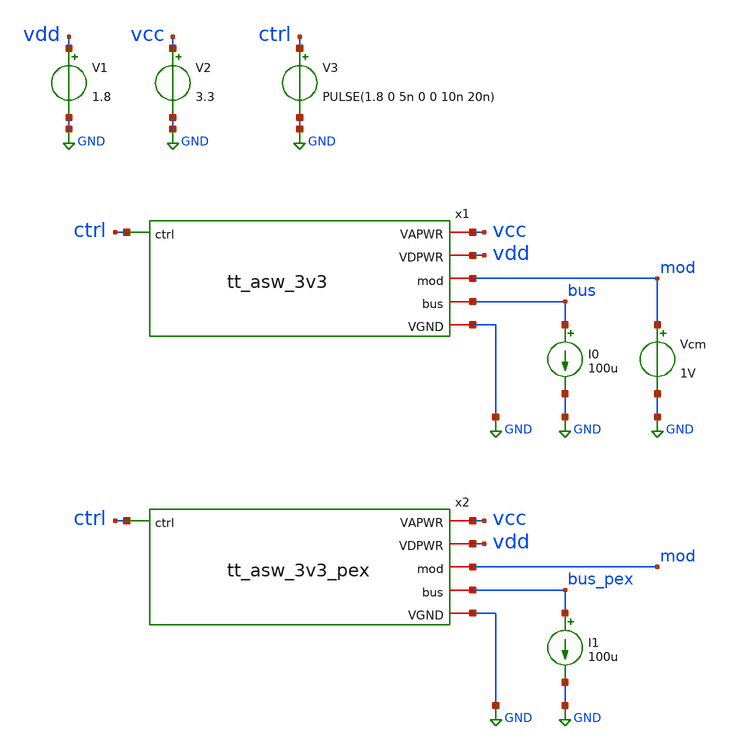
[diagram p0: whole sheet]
** sch_path: asw/tt_asw_3v3/xschem/tb_rdson.sch
**.subckt tb_rdson
x1 GND vdd vcc ctrl mod bus tt_asw_3v3
V2 vcc GND 3.3
Vcm mod GND 1V
I0 bus GND 100u
V3 ctrl GND PULSE(1.8 0 5n 0 0 10n 20n)
V1 vdd GND 1.8
x2 GND vdd vcc ctrl mod bus_pex tt_asw_3v3_pex
I1 bus_pex GND 100u
**** begin user architecture code

** opencircuitdesign pdks install
.lib $::SKYWATER_MODELS/sky130.lib.spice tt
.include $::SKYWATER_STDCELLS/sky130_fd_sc_hd.spice





.param mc_mm_switch=0
.control
tran 10p 100n
plot ctrl x1.tgon x1.tgon_n
dc Vcm 0 3.3 0.01
plot ((v(mod) - v(bus)) / 100u) ((v(mod) - v(bus_pex)) / 100u)
write tb_rdson.raw
*quit 0
.endc
.end


**** end user architecture code
**.ends

* expanding   symbol:  tt_asw_3v3.sym # of pins=6
** sym_path: asw/sky130/tt_asw_3v3/xschem/tt_asw_3v3.sym
** sch_path: asw/sky130/tt_asw_3v3/xschem/tt_asw_3v3.sch
.subckt tt_asw_3v3 VGND VDPWR VAPWR ctrl mod bus
*.iopin mod
*.iopin bus
*.ipin ctrl
*.iopin VGND
*.iopin VDPWR
*.iopin VAPWR
XM1 tgon_n net2 VAPWR VAPWR sky130_fd_pr__pfet_g5v0d10v5 L=0.5 W=0.84 nf=1 ad='int((nf+1)/2) * W/nf * 0.29'
+ as='int((nf+2)/2) * W/nf * 0.29' pd='2*int((nf+1)/2) * (W/nf + 0.29)' ps='2*int((nf+2)/2) * (W/nf + 0.29)'
+ nrd='0.29 / W' nrs='0.29 / W' sa=0 sb=0 sd=0 mult=1 m=1
XM2 tgon_n net2 VGND VGND sky130_fd_pr__nfet_g5v0d10v5 L=0.5 W=0.42 nf=1 ad='int((nf+1)/2) * W/nf * 0.29'
+ as='int((nf+2)/2) * W/nf * 0.29' pd='2*int((nf+1)/2) * (W/nf + 0.29)' ps='2*int((nf+2)/2) * (W/nf + 0.29)'
+ nrd='0.29 / W' nrs='0.29 / W' sa=0 sb=0 sd=0 mult=1 m=1
XM3 tgon net1 VAPWR VAPWR sky130_fd_pr__pfet_g5v0d10v5 L=0.5 W=0.84 nf=1 ad='int((nf+1)/2) * W/nf * 0.29'
+ as='int((nf+2)/2) * W/nf * 0.29' pd='2*int((nf+1)/2) * (W/nf + 0.29)' ps='2*int((nf+2)/2) * (W/nf + 0.29)'
+ nrd='0.29 / W' nrs='0.29 / W' sa=0 sb=0 sd=0 mult=1 m=1
XM4 tgon net1 VGND VGND sky130_fd_pr__nfet_g5v0d10v5 L=0.5 W=0.42 nf=1 ad='int((nf+1)/2) * W/nf * 0.29'
+ as='int((nf+2)/2) * W/nf * 0.29' pd='2*int((nf+1)/2) * (W/nf + 0.29)' ps='2*int((nf+2)/2) * (W/nf + 0.29)'
+ nrd='0.29 / W' nrs='0.29 / W' sa=0 sb=0 sd=0 mult=1 m=1
XM5 bus tgon_n mod VAPWR sky130_fd_pr__pfet_g5v0d10v5 L=0.5 W=180 nf=18 ad='int((nf+1)/2) * W/nf * 0.29'
+ as='int((nf+2)/2) * W/nf * 0.29' pd='2*int((nf+1)/2) * (W/nf + 0.29)' ps='2*int((nf+2)/2) * (W/nf + 0.29)'
+ nrd='0.29 / W' nrs='0.29 / W' sa=0 sb=0 sd=0 mult=1 m=1
XM6 bus tgon mod VGND sky130_fd_pr__nfet_g5v0d10v5 L=0.5 W=60 nf=12 ad='int((nf+1)/2) * W/nf * 0.29'
+ as='int((nf+2)/2) * W/nf * 0.29' pd='2*int((nf+1)/2) * (W/nf + 0.29)' ps='2*int((nf+2)/2) * (W/nf + 0.29)'
+ nrd='0.29 / W' nrs='0.29 / W' sa=0 sb=0 sd=0 mult=1 m=1
XM7 ctrl_n ctrl VGND VGND sky130_fd_pr__nfet_01v8 L=0.15 W=0.42 nf=1 ad='int((nf+1)/2) * W/nf * 0.29'
+ as='int((nf+2)/2) * W/nf * 0.29' pd='2*int((nf+1)/2) * (W/nf + 0.29)' ps='2*int((nf+2)/2) * (W/nf + 0.29)'
+ nrd='0.29 / W' nrs='0.29 / W' sa=0 sb=0 sd=0 mult=1 m=1
XM8 ctrl_n ctrl VDPWR VDPWR sky130_fd_pr__pfet_01v8_hvt L=0.15 W=1 nf=1 ad='int((nf+1)/2) * W/nf * 0.29'
+ as='int((nf+2)/2) * W/nf * 0.29' pd='2*int((nf+1)/2) * (W/nf + 0.29)' ps='2*int((nf+2)/2) * (W/nf + 0.29)'
+ nrd='0.29 / W' nrs='0.29 / W' sa=0 sb=0 sd=0 mult=1 m=1
XM9 net1 ctrl VGND VGND sky130_fd_pr__nfet_g5v0d10v5 L=0.5 W=0.42 nf=1 ad='int((nf+1)/2) * W/nf * 0.29'
+ as='int((nf+2)/2) * W/nf * 0.29' pd='2*int((nf+1)/2) * (W/nf + 0.29)' ps='2*int((nf+2)/2) * (W/nf + 0.29)'
+ nrd='0.29 / W' nrs='0.29 / W' sa=0 sb=0 sd=0 mult=1 m=1
XM10 net2 ctrl_n VGND VGND sky130_fd_pr__nfet_g5v0d10v5 L=0.5 W=0.42 nf=1 ad='int((nf+1)/2) * W/nf * 0.29'
+ as='int((nf+2)/2) * W/nf * 0.29' pd='2*int((nf+1)/2) * (W/nf + 0.29)' ps='2*int((nf+2)/2) * (W/nf + 0.29)'
+ nrd='0.29 / W' nrs='0.29 / W' sa=0 sb=0 sd=0 mult=1 m=1
XM11 net1 net2 net3 VAPWR sky130_fd_pr__pfet_g5v0d10v5 L=0.5 W=0.42 nf=1 ad='int((nf+1)/2) * W/nf * 0.29'
+ as='int((nf+2)/2) * W/nf * 0.29' pd='2*int((nf+1)/2) * (W/nf + 0.29)' ps='2*int((nf+2)/2) * (W/nf + 0.29)'
+ nrd='0.29 / W' nrs='0.29 / W' sa=0 sb=0 sd=0 mult=1 m=1
XM12 net2 net1 net4 VAPWR sky130_fd_pr__pfet_g5v0d10v5 L=0.5 W=0.42 nf=1 ad='int((nf+1)/2) * W/nf * 0.29'
+ as='int((nf+2)/2) * W/nf * 0.29' pd='2*int((nf+1)/2) * (W/nf + 0.29)' ps='2*int((nf+2)/2) * (W/nf + 0.29)'
+ nrd='0.29 / W' nrs='0.29 / W' sa=0 sb=0 sd=0 mult=1 m=1
XM13 net3 net1 VAPWR VAPWR sky130_fd_pr__pfet_g5v0d10v5 L=0.5 W=0.42 nf=1 ad='int((nf+1)/2) * W/nf * 0.29'
+ as='int((nf+2)/2) * W/nf * 0.29' pd='2*int((nf+1)/2) * (W/nf + 0.29)' ps='2*int((nf+2)/2) * (W/nf + 0.29)'
+ nrd='0.29 / W' nrs='0.29 / W' sa=0 sb=0 sd=0 mult=1 m=1
XM14 net4 net2 VAPWR VAPWR sky130_fd_pr__pfet_g5v0d10v5 L=0.5 W=0.42 nf=1 ad='int((nf+1)/2) * W/nf * 0.29'
+ as='int((nf+2)/2) * W/nf * 0.29' pd='2*int((nf+1)/2) * (W/nf + 0.29)' ps='2*int((nf+2)/2) * (W/nf + 0.29)'
+ nrd='0.29 / W' nrs='0.29 / W' sa=0 sb=0 sd=0 mult=1 m=1
.ends


* expanding   symbol:  tt_asw_3v3_pex.sym # of pins=6
** sym_path: asw/sky130/tt_asw_3v3/xschem/tt_asw_3v3.sym
.include [file normalize ../mag/tt_asw_3v3.pex.spice]
.GLOBAL GND
.end
